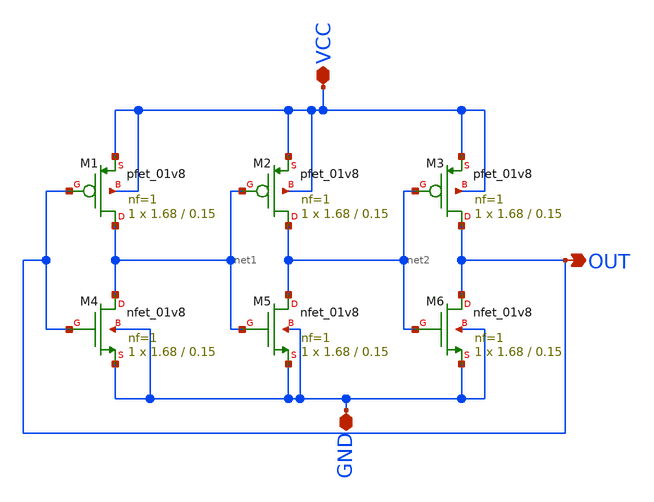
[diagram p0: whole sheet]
** sch_path: Week 4/xschem_comparator/ring_oscillator.sch
**.subckt ring_oscillator OUT VCC GND
*.opin OUT
*.iopin VCC
*.iopin GND
XM1 net1 OUT VCC VCC sky130_fd_pr__pfet_01v8 L=0.15 W=1.68 nf=1 ad='int((nf+1)/2) * W/nf * 0.29' as='int((nf+2)/2) * W/nf * 0.29'
+ pd='2*int((nf+1)/2) * (W/nf + 0.29)' ps='2*int((nf+2)/2) * (W/nf + 0.29)' nrd='0.29 / W' nrs='0.29 / W'
+ sa=0 sb=0 sd=0 mult=1 m=1
XM2 net2 net1 VCC VCC sky130_fd_pr__pfet_01v8 L=0.15 W=1.68 nf=1 ad='int((nf+1)/2) * W/nf * 0.29' as='int((nf+2)/2) * W/nf * 0.29'
+ pd='2*int((nf+1)/2) * (W/nf + 0.29)' ps='2*int((nf+2)/2) * (W/nf + 0.29)' nrd='0.29 / W' nrs='0.29 / W'
+ sa=0 sb=0 sd=0 mult=1 m=1
XM3 OUT net2 VCC VCC sky130_fd_pr__pfet_01v8 L=0.15 W=1.68 nf=1 ad='int((nf+1)/2) * W/nf * 0.29' as='int((nf+2)/2) * W/nf * 0.29'
+ pd='2*int((nf+1)/2) * (W/nf + 0.29)' ps='2*int((nf+2)/2) * (W/nf + 0.29)' nrd='0.29 / W' nrs='0.29 / W'
+ sa=0 sb=0 sd=0 mult=1 m=1
XM4 net1 OUT GND GND sky130_fd_pr__nfet_01v8 L=0.15 W=1.68 nf=1 ad='int((nf+1)/2) * W/nf * 0.29' as='int((nf+2)/2) * W/nf * 0.29'
+ pd='2*int((nf+1)/2) * (W/nf + 0.29)' ps='2*int((nf+2)/2) * (W/nf + 0.29)' nrd='0.29 / W' nrs='0.29 / W'
+ sa=0 sb=0 sd=0 mult=1 m=1
XM5 net2 net1 GND GND sky130_fd_pr__nfet_01v8 L=0.15 W=1.68 nf=1 ad='int((nf+1)/2) * W/nf * 0.29' as='int((nf+2)/2) * W/nf * 0.29'
+ pd='2*int((nf+1)/2) * (W/nf + 0.29)' ps='2*int((nf+2)/2) * (W/nf + 0.29)' nrd='0.29 / W' nrs='0.29 / W'
+ sa=0 sb=0 sd=0 mult=1 m=1
XM6 OUT net2 GND GND sky130_fd_pr__nfet_01v8 L=0.15 W=1.68 nf=1 ad='int((nf+1)/2) * W/nf * 0.29' as='int((nf+2)/2) * W/nf * 0.29'
+ pd='2*int((nf+1)/2) * (W/nf + 0.29)' ps='2*int((nf+2)/2) * (W/nf + 0.29)' nrd='0.29 / W' nrs='0.29 / W'
+ sa=0 sb=0 sd=0 mult=1 m=1
**.ends
.end
